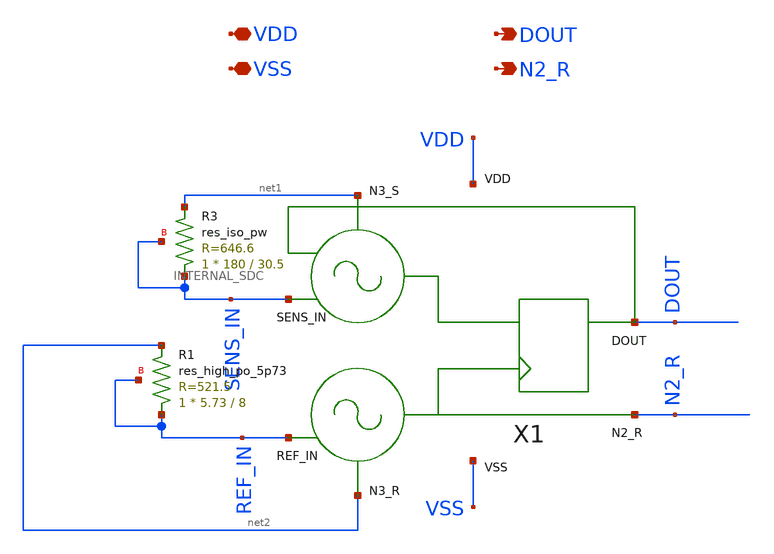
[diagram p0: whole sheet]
** sch_path: modules/SDC/symbol/SDC.sch
**.subckt SDC VDD VSS DOUT N2_R
*.iopin VDD
*.iopin VSS
*.opin DOUT
*.opin N2_R
X1 SENS_IN REF_IN DOUT VDD VSS net1 net2 N2_R INTERNAL_SDC
XR1 REF_IN net2 REF_IN sky130_fd_pr__res_high_po_5p73 L=8 mult=1 m=1
XR3 SENS_IN net1 SENS_IN sky130_fd_pr__res_iso_pw W=180 L=30.5 m=1
**.ends
.end
